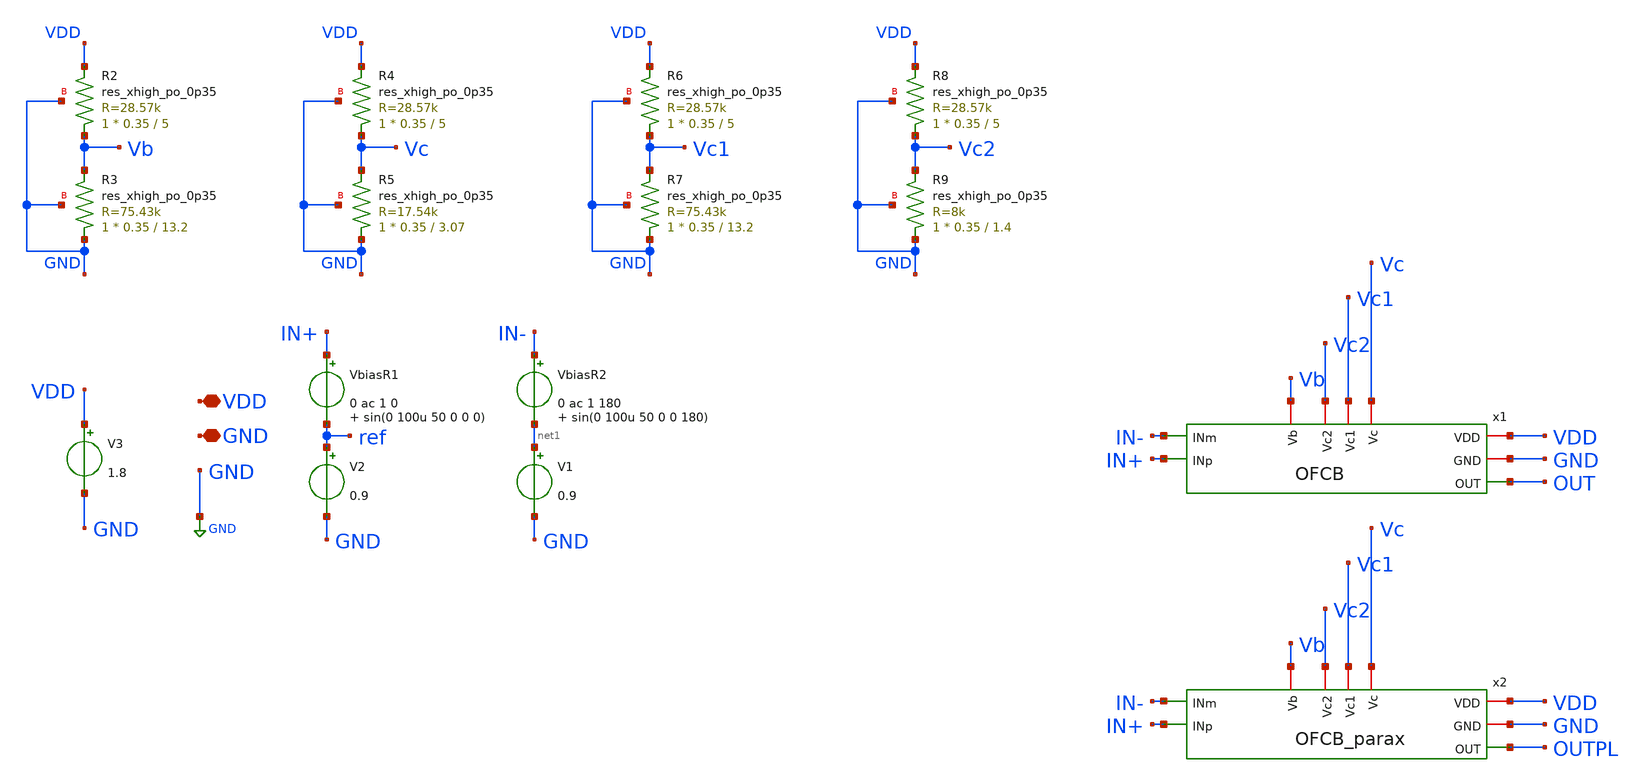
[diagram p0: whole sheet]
** sch_path: xschem/OFCBPL_MC.sch
**.subckt OFCBPL_MC VDD GND
*.iopin VDD
*.iopin GND
x1 Vb VDD GND Vc2 OUT IN+ IN- Vc1 Vc OFCB
x2 Vb VDD GND Vc2 OUTPL IN+ IN- Vc1 Vc OFCB_parax
VbiasR1 IN+ ref 0 ac 1 0 sin(0 100u 50 0 0 0)
V2 ref GND 0.9
V3 VDD GND 1.8
XR2 Vb VDD GND sky130_fd_pr__res_xhigh_po_0p35 L=5 mult=1 m=1
XR3 GND Vb GND sky130_fd_pr__res_xhigh_po_0p35 L=13.2 mult=1 m=1
XR4 Vc VDD GND sky130_fd_pr__res_xhigh_po_0p35 L=5 mult=1 m=1
XR5 GND Vc GND sky130_fd_pr__res_xhigh_po_0p35 L=3.07 mult=1 m=1
XR6 Vc1 VDD GND sky130_fd_pr__res_xhigh_po_0p35 L=5 mult=1 m=1
XR7 GND Vc1 GND sky130_fd_pr__res_xhigh_po_0p35 L=13.2 mult=1 m=1
XR8 Vc2 VDD GND sky130_fd_pr__res_xhigh_po_0p35 L=5 mult=1 m=1
XR9 GND Vc2 GND sky130_fd_pr__res_xhigh_po_0p35 L=1.4 mult=1 m=1
VbiasR2 IN- net1 0 ac 1 180 sin(0 100u 50 0 0 180)
V1 net1 GND 0.9
**** begin user architecture code



.control
    set wr_vecnames
    set wr_singlescale

    * 1. Pulizia iniziale del file per evitare di appendere a vecchie simulazioni
    shell rm -f mcAC_out.txt

    * Impostazioni per il salvataggio pulito
    set appendwrite

    let mc_runs = 200
    let run = 1

    dowhile run <= mc_runs
        * 2. FORZA IL CAMBIO DEL PARAMETRO CASUALE
        * Impostiamo il seed basandoci sul numero del run.
        * Questo garantisce che 'reset' peschi valori diversi ogni volta.
        set seed = $&run

        * 3. RESETTA LA RETE
        * Ricarica i parametri gauss() o unif() definiti nei modelli/istanze
        reset

        * 4. ESECUZIONE SIMULAZIONE AC
        * L'offset di 0.9V deve essere già presente nel tuo generatore V_in (DC 0.9)
        ac dec 10 1 1e9

        * 5. SALVATAGGIO DATI
        * Calcoliamo il vettore e lo scriviamo. 'appendwrite' lo mette in coda.
        let gain_db = db(v(OUTPL))
        wrdata mcAC_out.txt gain_db

        * 6. PULIZIA E AVANZAMENTO
        * Distrugge il plot attuale per non saturare la RAM
        destroy all

        * Feedback a video (non scrive su file, serve a te per monitorare)
        echo

        let run = run + 1
    end
.endc



.lib $::SKYWATER_MODELS/sky130.lib.spice tt_mm
**** end user architecture code
**.ends

* expanding   symbol:  OFCB.sym # of pins=9
** sym_path: xschem/OFCB.sym
** sch_path: xschem/OFCB.sch
.subckt OFCB Vb VDD GND Vc2 OUT INp INm Vc1 Vc
*.iopin VDD
*.iopin GND
*.opin OUT
*.ipin INp
*.ipin INm
*.iopin Vc2
*.iopin Vc1
*.iopin Vc
*.iopin Vb
XM11 S Vb VDD VDD sky130_fd_pr__pfet_01v8_lvt L=1 W=60 nf=6 ad='int((nf+1)/2) * W/nf * 0.29' as='int((nf+2)/2)
+ * W/nf * 0.29' pd='2*int((nf+1)/2) * (W/nf + 0.29)' ps='2*int((nf+2)/2) * (W/nf + 0.29)' nrd='0.29 /
+ W' nrs='0.29 / W' sa=0 sb=0 sd=0 mult=2 m=2
XM1 D1 INp S S sky130_fd_pr__pfet_01v8_lvt L=10 W=25 nf=2 ad='int((nf+1)/2) * W/nf * 0.29' as='int((nf+2)/2)
+ * W/nf * 0.29' pd='2*int((nf+1)/2) * (W/nf + 0.29)' ps='2*int((nf+2)/2) * (W/nf + 0.29)' nrd='0.29 /
+ W' nrs='0.29 / W' sa=0 sb=0 sd=0 mult=2 m=2
XM2 D2 INm S S sky130_fd_pr__pfet_01v8_lvt L=10 W=25 nf=2 ad='int((nf+1)/2) * W/nf * 0.29' as='int((nf+2)/2)
+ * W/nf * 0.29' pd='2*int((nf+1)/2) * (W/nf + 0.29)' ps='2*int((nf+2)/2) * (W/nf + 0.29)' nrd='0.29 /
+ W' nrs='0.29 / W' sa=0 sb=0 sd=0 mult=2 m=2
XM3 OUT Vc1 D2 GND sky130_fd_pr__nfet_01v8_lvt L=1 W=4 nf=1 ad='int((nf+1)/2) * W/nf * 0.29' as='int((nf+2)/2)
+ * W/nf * 0.29' pd='2*int((nf+1)/2) * (W/nf + 0.29)' ps='2*int((nf+2)/2) * (W/nf + 0.29)' nrd='0.29 /
+ W' nrs='0.29 / W' sa=0 sb=0 sd=0 mult=1 m=1
XM4 D2 Vc GND GND sky130_fd_pr__nfet_01v8_lvt L=1 W=2.8 nf=1 ad='int((nf+1)/2) * W/nf * 0.29' as='int((nf+2)/2)
+ * W/nf * 0.29' pd='2*int((nf+1)/2) * (W/nf + 0.29)' ps='2*int((nf+2)/2) * (W/nf + 0.29)' nrd='0.29 /
+ W' nrs='0.29 / W' sa=0 sb=0 sd=0 mult=1 m=1
XM5 D1 Vc GND GND sky130_fd_pr__nfet_01v8_lvt L=1 W=2.8 nf=1 ad='int((nf+1)/2) * W/nf * 0.29' as='int((nf+2)/2)
+ * W/nf * 0.29' pd='2*int((nf+1)/2) * (W/nf + 0.29)' ps='2*int((nf+2)/2) * (W/nf + 0.29)' nrd='0.29 /
+ W' nrs='0.29 / W' sa=0 sb=0 sd=0 mult=1 m=1
XM6 G Vc1 D1 GND sky130_fd_pr__nfet_01v8_lvt L=1 W=4 nf=1 ad='int((nf+1)/2) * W/nf * 0.29' as='int((nf+2)/2)
+ * W/nf * 0.29' pd='2*int((nf+1)/2) * (W/nf + 0.29)' ps='2*int((nf+2)/2) * (W/nf + 0.29)' nrd='0.29 /
+ W' nrs='0.29 / W' sa=0 sb=0 sd=0 mult=1 m=1
XM7 G Vc2 D9 D9 sky130_fd_pr__pfet_01v8_lvt L=2.23 W=4 nf=1 ad='int((nf+1)/2) * W/nf * 0.29' as='int((nf+2)/2)
+ * W/nf * 0.29' pd='2*int((nf+1)/2) * (W/nf + 0.29)' ps='2*int((nf+2)/2) * (W/nf + 0.29)' nrd='0.29 /
+ W' nrs='0.29 / W' sa=0 sb=0 sd=0 mult=1 m=1
XM9 D9 G VDD VDD sky130_fd_pr__pfet_01v8_lvt L=2.23 W=3.85 nf=1 ad='int((nf+1)/2) * W/nf * 0.29' as='int((nf+2)/2)
+ * W/nf * 0.29' pd='2*int((nf+1)/2) * (W/nf + 0.29)' ps='2*int((nf+2)/2) * (W/nf + 0.29)' nrd='0.29 /
+ W' nrs='0.29 / W' sa=0 sb=0 sd=0 mult=1 m=1
XM8 D10 G VDD VDD sky130_fd_pr__pfet_01v8_lvt L=2.23 W=3.85 nf=1 ad='int((nf+1)/2) * W/nf * 0.29' as='int((nf+2)/2)
+ * W/nf * 0.29' pd='2*int((nf+1)/2) * (W/nf + 0.29)' ps='2*int((nf+2)/2) * (W/nf + 0.29)' nrd='0.29 /
+ W' nrs='0.29 / W' sa=0 sb=0 sd=0 mult=1 m=1
XM10 OUT Vc2 D10 D10 sky130_fd_pr__pfet_01v8_lvt L=2.23 W=4 nf=1 ad='int((nf+1)/2) * W/nf * 0.29' as='int((nf+2)/2)
+ * W/nf * 0.29' pd='2*int((nf+1)/2) * (W/nf + 0.29)' ps='2*int((nf+2)/2) * (W/nf + 0.29)' nrd='0.29 /
+ W' nrs='0.29 / W' sa=0 sb=0 sd=0 mult=1 m=1
XC1 OUT D1 sky130_fd_pr__cap_mim_m3_1 W=22.4 L=22.4 MF=2 m=2
.ends


* expanding   symbol:  OFCB_parax.sym # of pins=9
** sym_path: xschem/OFCB.sym
.include [file normalize ../mag/OFCB.sim.spice]
.GLOBAL GND
.end
